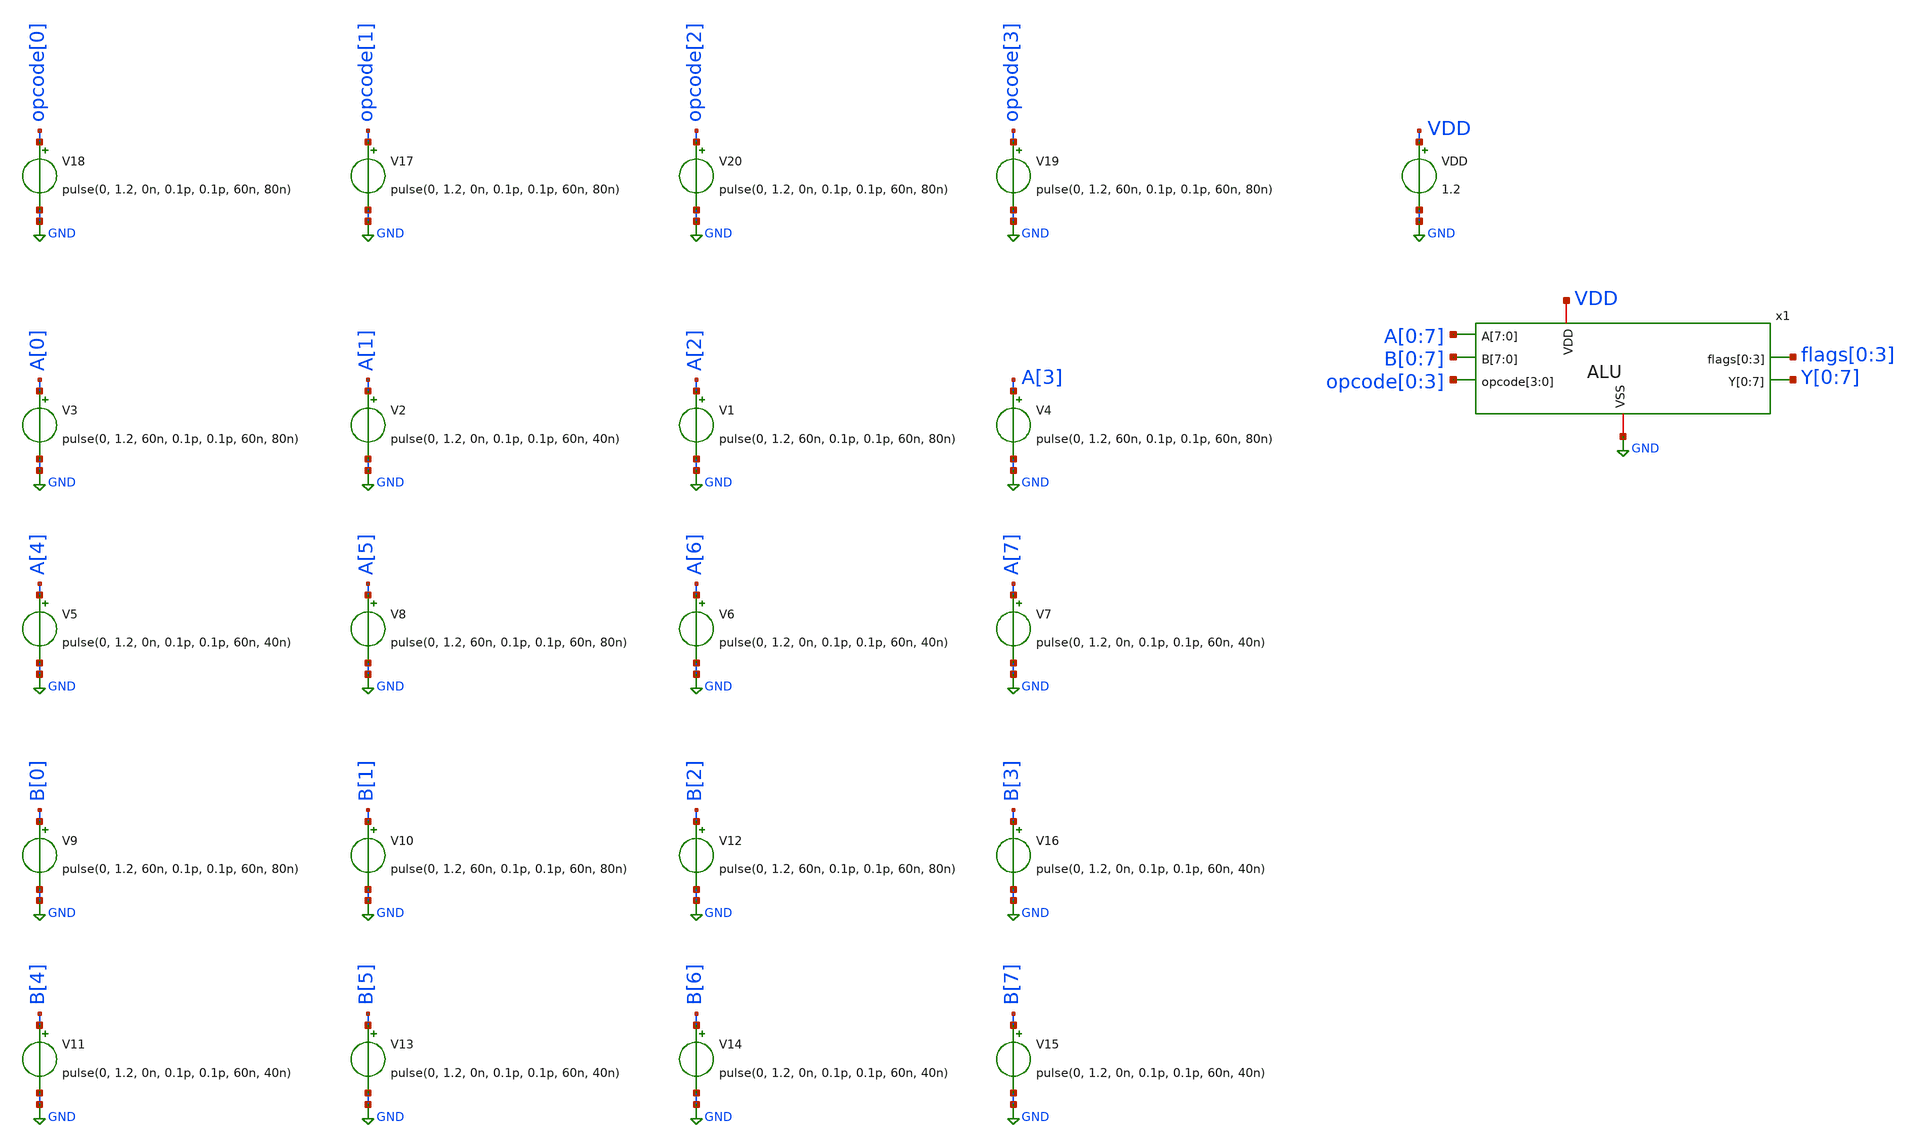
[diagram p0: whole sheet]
** sch_path: design/ALU/alu_tb.sch
**.subckt alu_tb
V3 A[0] GND pulse(0, 1.2, 60n, 0.1p, 0.1p, 60n, 80n)
V2 A[1] GND pulse(0, 1.2, 0n, 0.1p, 0.1p, 60n, 40n)
V18 opcode[0] GND pulse(0, 1.2, 0n, 0.1p, 0.1p, 60n, 80n)
V19 opcode[3] GND pulse(0, 1.2, 60n, 0.1p, 0.1p, 60n, 80n)
x1 A[0] A[1] A[2] A[3] A[4] A[5] A[6] A[7] B[0] B[1] B[2] B[3] B[4] B[5] B[6] B[7] opcode[0]
+ opcode[1] opcode[2] opcode[3] GND VDD flags[0] flags[1] flags[2] flags[3] Y[0] Y[1] Y[2] Y[3] Y[4] Y[5] Y[6]
+ Y[7] ALU
VDD VDD GND 1.2
V17 opcode[1] GND pulse(0, 1.2, 0n, 0.1p, 0.1p, 60n, 80n)
V20 opcode[2] GND pulse(0, 1.2, 0n, 0.1p, 0.1p, 60n, 80n)
V1 A[2] GND pulse(0, 1.2, 60n, 0.1p, 0.1p, 60n, 80n)
V4 A[3] GND pulse(0, 1.2, 60n, 0.1p, 0.1p, 60n, 80n)
V8 A[5] GND pulse(0, 1.2, 60n, 0.1p, 0.1p, 60n, 80n)
V5 A[4] GND pulse(0, 1.2, 0n, 0.1p, 0.1p, 60n, 40n)
V6 A[6] GND pulse(0, 1.2, 0n, 0.1p, 0.1p, 60n, 40n)
V7 A[7] GND pulse(0, 1.2, 0n, 0.1p, 0.1p, 60n, 40n)
V9 B[0] GND pulse(0, 1.2, 60n, 0.1p, 0.1p, 60n, 80n)
V10 B[1] GND pulse(0, 1.2, 60n, 0.1p, 0.1p, 60n, 80n)
V12 B[2] GND pulse(0, 1.2, 60n, 0.1p, 0.1p, 60n, 80n)
V11 B[4] GND pulse(0, 1.2, 0n, 0.1p, 0.1p, 60n, 40n)
V13 B[5] GND pulse(0, 1.2, 0n, 0.1p, 0.1p, 60n, 40n)
V14 B[6] GND pulse(0, 1.2, 0n, 0.1p, 0.1p, 60n, 40n)
V15 B[7] GND pulse(0, 1.2, 0n, 0.1p, 0.1p, 60n, 40n)
V16 B[3] GND pulse(0, 1.2, 0n, 0.1p, 0.1p, 60n, 40n)
**** begin user architecture code

** opencircuitdesign pdks install
.lib $::SKYWATER_MODELS/sky130.lib.spice tt_mm



.control
save all

set color0 = white
tran 10p 100n

plot "a[0]" "a[1]"+2 "a[2]"+4 "a[3]"+6 "a[4]"+8 "a[5]"+10 "a[6]"+12 "a[7]"+14
plot "b[0]" "b[1]"+2 "b[2]"+4 "b[3]"+6 "b[4]"+8 "b[5]"+10 "b[6]"+12 "b[7]"+14
plot "y[0]" "y[1]"+2 "y[2]"+4 "y[3]"+6 "y[4]"+8 "y[5]"+10 "y[6]"+12 "y[7]"+14
plot "opcode[0]" "opcode[1]"+2 "opcode[2]"+4 "opcode[3]"+6
plot "flags[0]" "flags[1]"+2 "flags[2]"+4 "flags[3]"+6
.endc

**** end user architecture code
**.ends
.GLOBAL GND
.end
